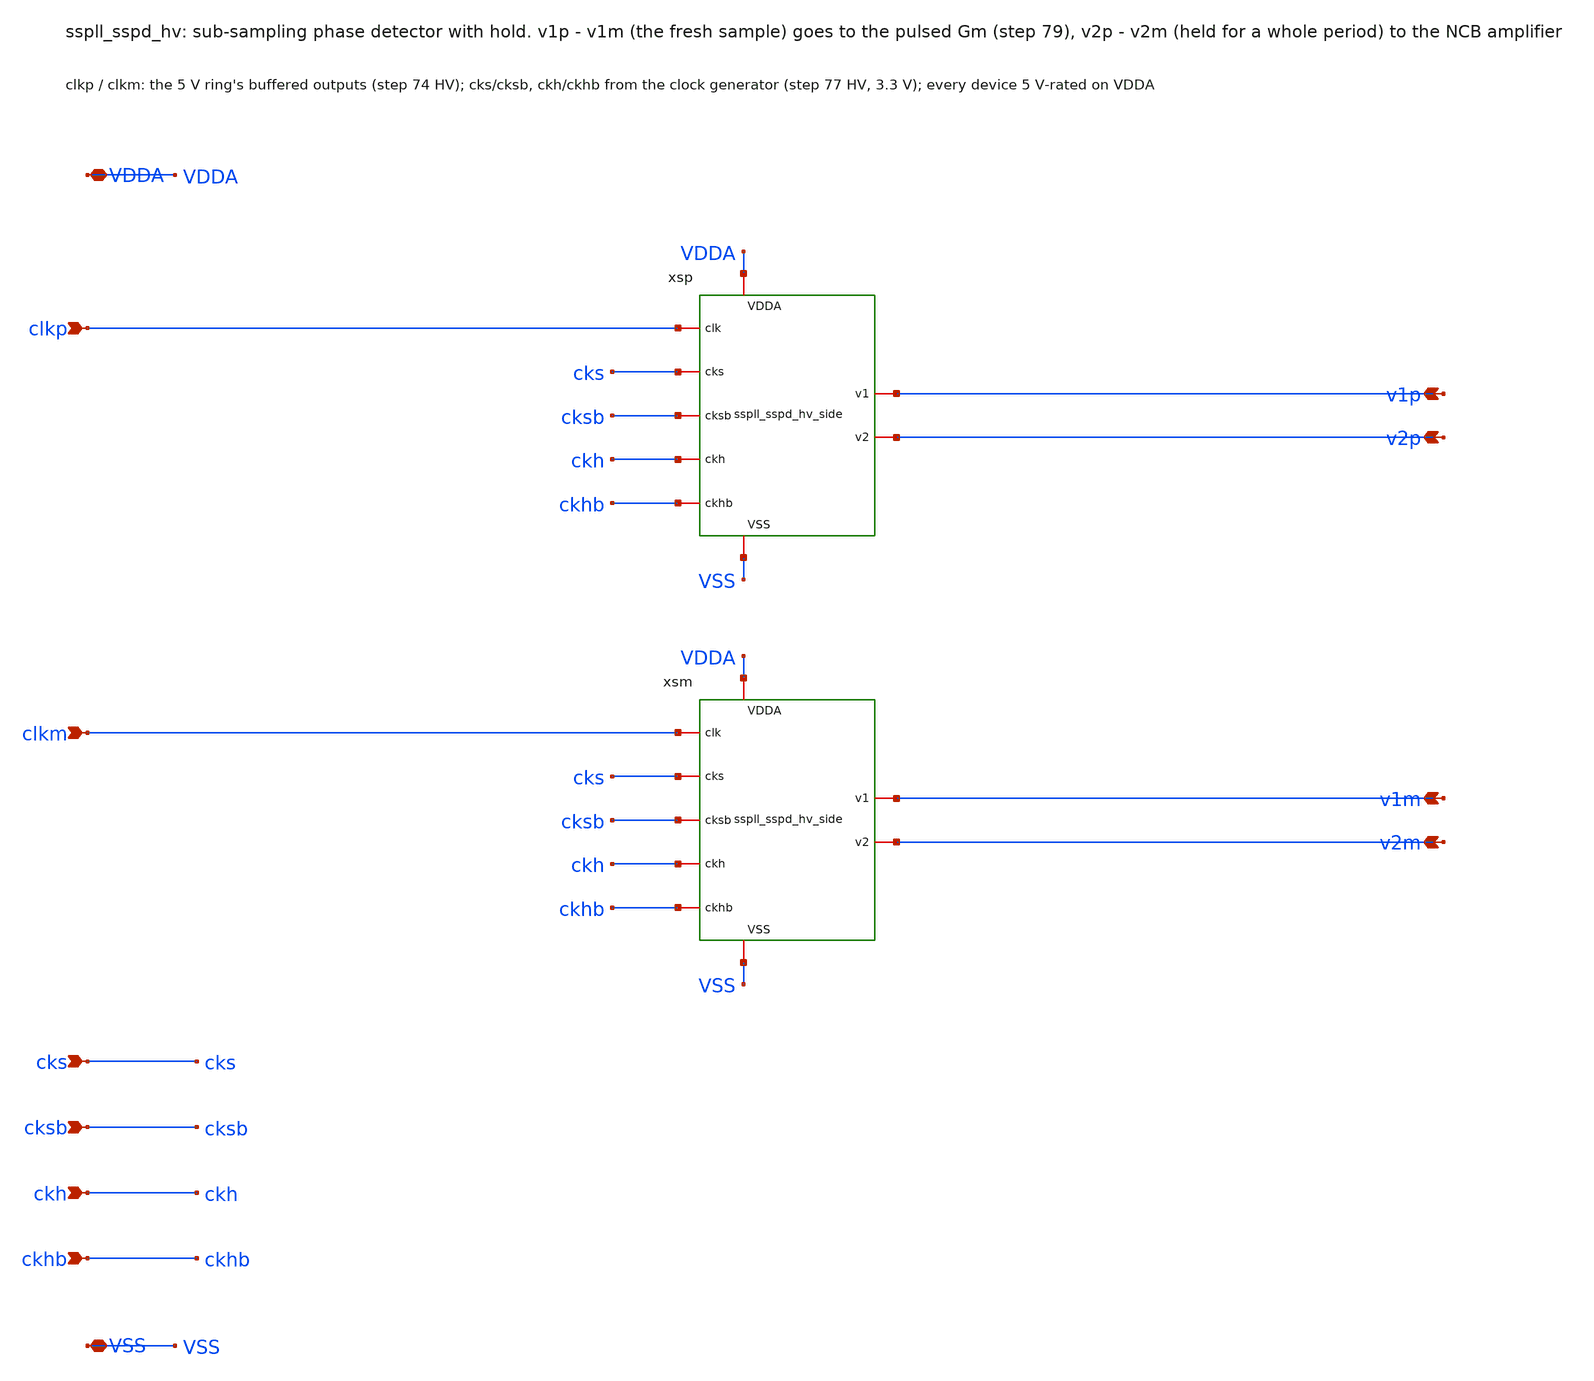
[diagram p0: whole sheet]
** sch_path: xschem/sspd_hv/sspll_sspd_hv.sch
**.subckt sspll_sspd_hv clkp clkm v1p v2p v1m v2m cks cksb ckh ckhb VDDA VSS
*.ipin clkp
*.ipin clkm
*.opin v1p
*.opin v2p
*.opin v1m
*.opin v2m
*.ipin cks
*.ipin cksb
*.ipin ckh
*.ipin ckhb
*.iopin VDDA
*.iopin VSS
xsp clkp cks cksb ckh ckhb v1p v2p VDDA VSS sspll_sspd_hv_side
xsm clkm cks cksb ckh ckhb v1m v2m VDDA VSS sspll_sspd_hv_side
**.ends
.end
